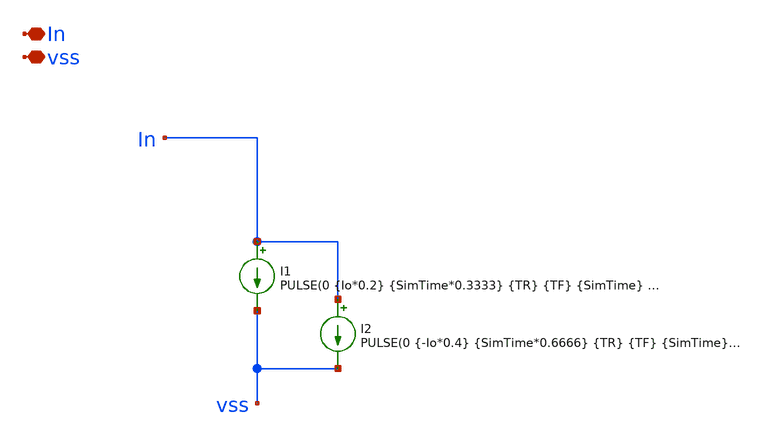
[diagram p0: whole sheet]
** sch_path: xschem/Dynamic_Load/Load.sch
**.subckt Load vss In
*.iopin vss
*.iopin In
I1 In vss PULSE(0 {Io*0.2} {SimTime*0.3333} {TR} {TF} {SimTime} {SimTime} 0)
I2 In vss PULSE(0 {-Io*0.4} {SimTime*0.6666} {TR} {TF} {SimTime} {SimTime} 0)
**.ends
.end
